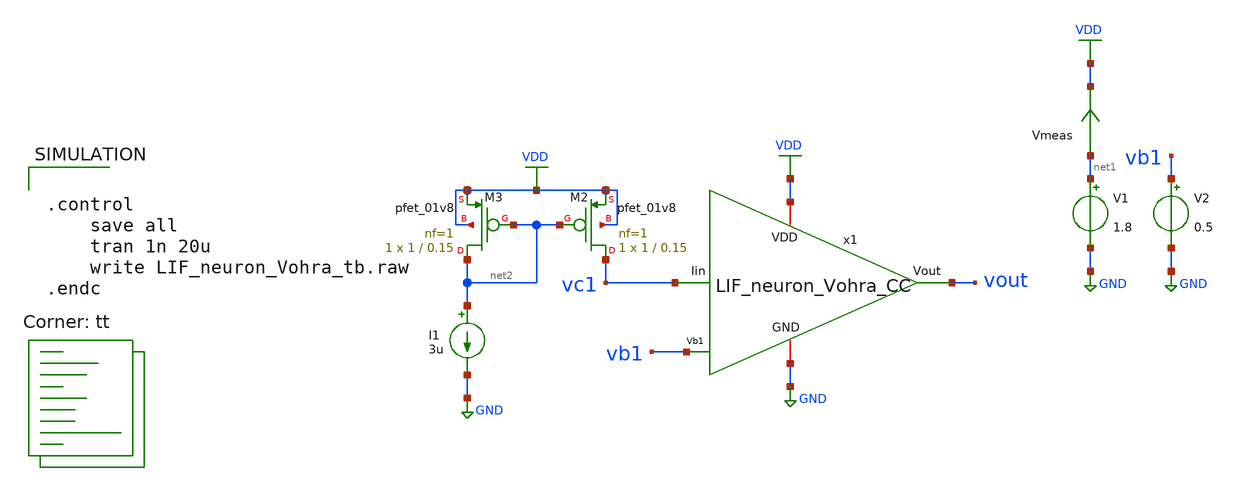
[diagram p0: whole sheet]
** sch_path: LIF_neuron/LIF_neuron_Vohra_CC_tb.sch
**.subckt LIF_neuron_Vohra_CC_tb
V1 net1 GND 1.8
V2 vb1 GND 0.5
x1 VDD vout vb1 GND vc1 LIF_neuron_Vohra_CC
I1 net2 GND 3u
XM2 vc1 net2 VDD VDD sky130_fd_pr__pfet_01v8 L=0.15 W=1 nf=1 ad='int((nf+1)/2) * W/nf * 0.29' as='int((nf+2)/2) * W/nf * 0.29'
+ pd='2*int((nf+1)/2) * (W/nf + 0.29)' ps='2*int((nf+2)/2) * (W/nf + 0.29)' nrd='0.29 / W' nrs='0.29 / W'
+ sa=0 sb=0 sd=0 mult=1 m=1
XM3 net2 net2 VDD VDD sky130_fd_pr__pfet_01v8 L=0.15 W=1 nf=1 ad='int((nf+1)/2) * W/nf * 0.29' as='int((nf+2)/2) * W/nf * 0.29'
+ pd='2*int((nf+1)/2) * (W/nf + 0.29)' ps='2*int((nf+2)/2) * (W/nf + 0.29)' nrd='0.29 / W' nrs='0.29 / W'
+ sa=0 sb=0 sd=0 mult=1 m=1
Vmeas net1 VDD 0
.save i(vmeas)
**** begin user architecture code


.control
	save all
	tran 1n 20u
	write LIF_neuron_Vohra_tb.raw
.endc


.lib $::SKYWATER_MODELS/sky130.lib.spice tt
**** end user architecture code
**.ends

* expanding   symbol:  /home/ricardo/RATT_repos/Proyectos_xschem/LIF_neuron/LIF_neuron_Vohra_CC.sym
*+ # of pins=5
** sym_path: LIF_neuron/LIF_neuron_Vohra_CC.sym
** sch_path: LIF_neuron/LIF_neuron_Vohra_CC.sch
.subckt LIF_neuron_Vohra_CC VDD Vout Vb1 GND Iin
*.iopin GND
*.ipin Vb1
*.iopin VDD
*.opin Vout
*.ipin Iin
XM8 net2 Vb1 GND GND sky130_fd_pr__nfet_01v8 L=0.5 W=5 nf=1 ad='int((nf+1)/2) * W/nf * 0.29' as='int((nf+2)/2) * W/nf * 0.29'
+ pd='2*int((nf+1)/2) * (W/nf + 0.29)' ps='2*int((nf+2)/2) * (W/nf + 0.29)' nrd='0.29 / W' nrs='0.29 / W'
+ sa=0 sb=0 sd=0 mult=1 m=1
XM7 rc net1 net2 GND sky130_fd_pr__nfet_01v8 L=1 W=1 nf=1 ad='int((nf+1)/2) * W/nf * 0.29' as='int((nf+2)/2) * W/nf * 0.29'
+ pd='2*int((nf+1)/2) * (W/nf + 0.29)' ps='2*int((nf+2)/2) * (W/nf + 0.29)' nrd='0.29 / W' nrs='0.29 / W'
+ sa=0 sb=0 sd=0 mult=1 m=1
XM6 rc net1 VDD VDD sky130_fd_pr__pfet_01v8 L=1 W=5 nf=1 ad='int((nf+1)/2) * W/nf * 0.29' as='int((nf+2)/2) * W/nf * 0.29'
+ pd='2*int((nf+1)/2) * (W/nf + 0.29)' ps='2*int((nf+2)/2) * (W/nf + 0.29)' nrd='0.29 / W' nrs='0.29 / W'
+ sa=0 sb=0 sd=0 mult=1 m=1
XCr rc GND sky130_fd_pr__cap_mim_m3_1 W=10 L=1 MF=1 m=1
XM9 Iin rc GND GND sky130_fd_pr__nfet_01v8 L=1 W=5 nf=1 ad='int((nf+1)/2) * W/nf * 0.29' as='int((nf+2)/2) * W/nf * 0.29'
+ pd='2*int((nf+1)/2) * (W/nf + 0.29)' ps='2*int((nf+2)/2) * (W/nf + 0.29)' nrd='0.29 / W' nrs='0.29 / W'
+ sa=0 sb=0 sd=0 mult=1 m=1
XCm Iin GND sky130_fd_pr__cap_mim_m3_1 W=30 L=1 MF=50 m=50
XM5 net3 Vout GND GND sky130_fd_pr__nfet_01v8 L=0.5 W=1 nf=1 ad='int((nf+1)/2) * W/nf * 0.29' as='int((nf+2)/2) * W/nf * 0.29'
+ pd='2*int((nf+1)/2) * (W/nf + 0.29)' ps='2*int((nf+2)/2) * (W/nf + 0.29)' nrd='0.29 / W' nrs='0.29 / W'
+ sa=0 sb=0 sd=0 mult=1 m=1
XM3 net1 Iin net3 GND sky130_fd_pr__nfet_01v8 L=1 W=1 nf=1 ad='int((nf+1)/2) * W/nf * 0.29' as='int((nf+2)/2) * W/nf * 0.29'
+ pd='2*int((nf+1)/2) * (W/nf + 0.29)' ps='2*int((nf+2)/2) * (W/nf + 0.29)' nrd='0.29 / W' nrs='0.29 / W'
+ sa=0 sb=0 sd=0 mult=1 m=1
XM1 net1 Iin VDD VDD sky130_fd_pr__pfet_01v8 L=1 W=1 nf=1 ad='int((nf+1)/2) * W/nf * 0.29' as='int((nf+2)/2) * W/nf * 0.29'
+ pd='2*int((nf+1)/2) * (W/nf + 0.29)' ps='2*int((nf+2)/2) * (W/nf + 0.29)' nrd='0.29 / W' nrs='0.29 / W'
+ sa=0 sb=0 sd=0 mult=1 m=1
XM4 Vout net1 net3 GND sky130_fd_pr__nfet_01v8 L=1 W=1 nf=1 ad='int((nf+1)/2) * W/nf * 0.29' as='int((nf+2)/2) * W/nf * 0.29'
+ pd='2*int((nf+1)/2) * (W/nf + 0.29)' ps='2*int((nf+2)/2) * (W/nf + 0.29)' nrd='0.29 / W' nrs='0.29 / W'
+ sa=0 sb=0 sd=0 mult=1 m=1
XM2 Vout net1 VDD VDD sky130_fd_pr__pfet_01v8 L=1 W=5 nf=1 ad='int((nf+1)/2) * W/nf * 0.29' as='int((nf+2)/2) * W/nf * 0.29'
+ pd='2*int((nf+1)/2) * (W/nf + 0.29)' ps='2*int((nf+2)/2) * (W/nf + 0.29)' nrd='0.29 / W' nrs='0.29 / W'
+ sa=0 sb=0 sd=0 mult=1 m=1
.ends

.GLOBAL GND
.GLOBAL VDD
.end
